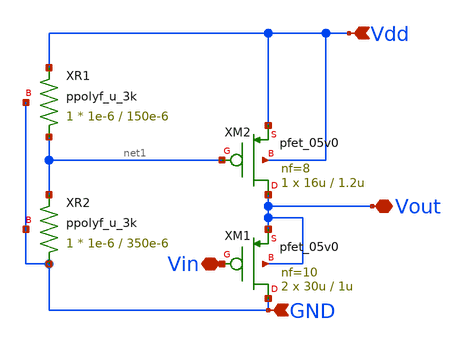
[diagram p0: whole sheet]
** sch_path: RN_buffer/buffer.sch
**.subckt buffer Vdd GND Vin Vout
*.ipin Vdd
*.ipin GND
*.iopin Vin
*.iopin Vout
XM1 GND Vin Vout Vout pfet_05v0 L=1u W=30u nf=10 ad='int((nf+1)/2) * W/nf * 0.18u' as='int((nf+2)/2) * W/nf * 0.18u'
+ pd='2*int((nf+1)/2) * (W/nf + 0.18u)' ps='2*int((nf+2)/2) * (W/nf + 0.18u)' nrd='0.18u / W' nrs='0.18u / W'
+ sa=0 sb=0 sd=0 m=2
XR1 net1 Vdd GND ppolyf_u_3k r_width=1e-6 r_length=150e-6 m=1
XR2 GND net1 GND ppolyf_u_3k r_width=1e-6 r_length=350e-6 m=1
XM2 Vout net1 Vdd Vdd pfet_05v0 L=1.2u W=16u nf=8 ad='int((nf+1)/2) * W/nf * 0.18u' as='int((nf+2)/2) * W/nf * 0.18u'
+ pd='2*int((nf+1)/2) * (W/nf + 0.18u)' ps='2*int((nf+2)/2) * (W/nf + 0.18u)' nrd='0.18u / W' nrs='0.18u / W'
+ sa=0 sb=0 sd=0 m=1
**.ends
.end
